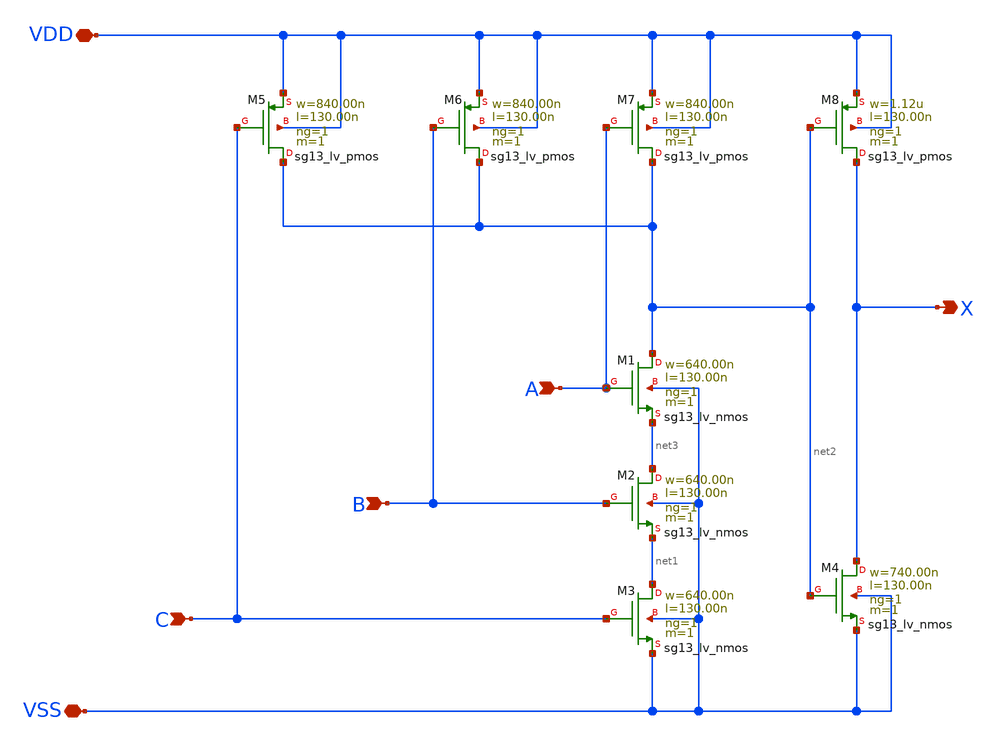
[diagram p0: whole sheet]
** sch_path: ihp-sg13g2/libs.tech/xschem/sg13g2_stdcells/sg13g2_and3_1.sch
**.subckt sg13g2_and3_1 X C B A VDD VSS
*.opin X
*.ipin C
*.ipin B
*.ipin A
*.iopin VDD
*.iopin VSS
XM1 net2 A net3 VSS sg13_lv_nmos w=640.00n l=130.00n ng=1 m=1 mm_ok=1
XM2 net3 B net1 VSS sg13_lv_nmos w=640.00n l=130.00n ng=1 m=1 mm_ok=1
XM3 net1 C VSS VSS sg13_lv_nmos w=640.00n l=130.00n ng=1 m=1 mm_ok=1
XM4 X net2 VSS VSS sg13_lv_nmos w=740.00n l=130.00n ng=1 m=1 mm_ok=1
XM5 net2 C VDD VDD sg13_lv_pmos w=840.00n l=130.00n ng=1 m=1 mm_ok=1
XM6 net2 B VDD VDD sg13_lv_pmos w=840.00n l=130.00n ng=1 m=1 mm_ok=1
XM7 net2 A VDD VDD sg13_lv_pmos w=840.00n l=130.00n ng=1 m=1 mm_ok=1
XM8 X net2 VDD VDD sg13_lv_pmos w=1.12u l=130.00n ng=1 m=1 mm_ok=1
**.ends
.end
